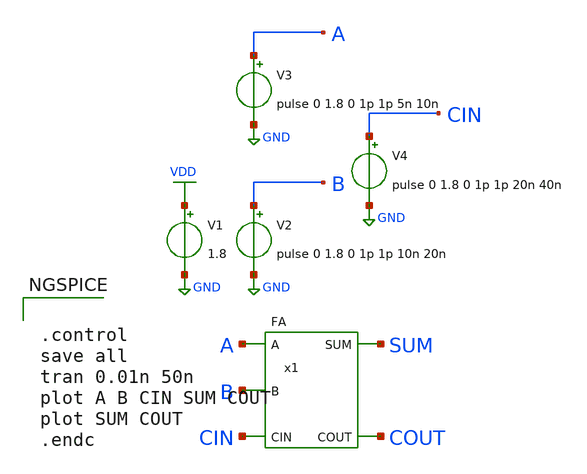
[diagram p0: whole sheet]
** sch_path: lib/xschem/test_FA.sch
**.subckt test_FA
V2 B GND pulse 0 1.8 0 1p 1p 10n 20n
V1 VDD GND 1.8
V3 A GND pulse 0 1.8 0 1p 1p 5n 10n
x1 SUM COUT A B CIN VDD GND FA
V4 CIN GND pulse 0 1.8 0 1p 1p 20n 40n
**** begin user architecture code

.lib $::SKYWATER_MODELS/sky130.lib.spice tt


**** end user architecture code
**.ends
.GLOBAL VDD
.GLOBAL GND
**** begin user architecture code


.control
save all
tran 0.01n 50n
plot A B CIN SUM COUT
plot SUM COUT
.endc


**** end user architecture code
.end
